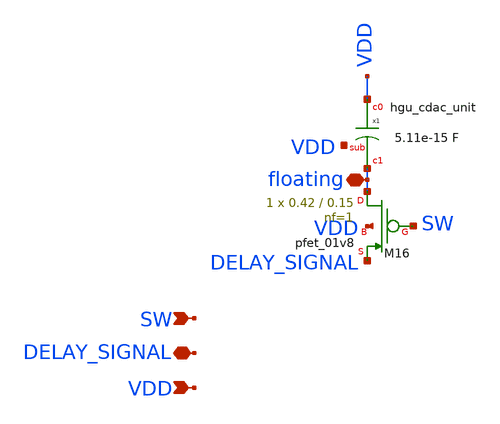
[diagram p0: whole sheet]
** sch_path: xschem/hgu_sw_cap_pmos.sch
**.subckt hgu_sw_cap_pmos SW VDD DELAY_SIGNAL floating
*.ipin SW
*.ipin VDD
*.iopin DELAY_SIGNAL
*.iopin floating
XM16 floating SW DELAY_SIGNAL VDD sky130_fd_pr__pfet_01v8 L=0.15 W=0.42 nf=1 ad='int((nf+1)/2) * W/nf * 0.29'
+ as='int((nf+2)/2) * W/nf * 0.29' pd='2*int((nf+1)/2) * (W/nf + 0.29)' ps='2*int((nf+2)/2) * (W/nf + 0.29)'
+ nrd='0.29 / W' nrs='0.29 / W' sa=0 sb=0 sd=0 mult=1 m=1
x1 VDD floating VDD hgu_cdac_unit
**.ends
.end
